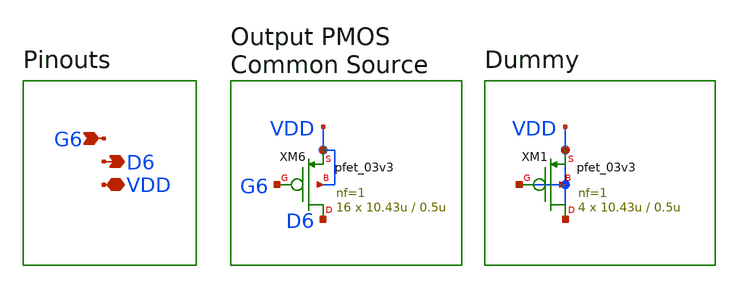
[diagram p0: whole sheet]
** sch_path: designs/libs/core_single_ended_ota/output_stage/output_stage.sch
**.subckt output_stage VDD G6 D6
*.iopin VDD
*.ipin G6
*.opin D6
XM6 D6 G6 VDD VDD pfet_03v3 L=0.5u W=10.43u nf=1 ad='int((nf+1)/2) * W/nf * 0.18u' as='int((nf+2)/2) * W/nf * 0.18u'
+ pd='2*int((nf+1)/2) * (W/nf + 0.18u)' ps='2*int((nf+2)/2) * (W/nf + 0.18u)' nrd='0.18u / W' nrs='0.18u / W'
+ sa=0 sb=0 sd=0 m=16
XM1 VDD VDD VDD VDD pfet_03v3 L=0.5u W=10.43u nf=1 ad='int((nf+1)/2) * W/nf * 0.18u' as='int((nf+2)/2) * W/nf * 0.18u'
+ pd='2*int((nf+1)/2) * (W/nf + 0.18u)' ps='2*int((nf+2)/2) * (W/nf + 0.18u)' nrd='0.18u / W' nrs='0.18u / W'
+ sa=0 sb=0 sd=0 m=4
**.ends
.end
